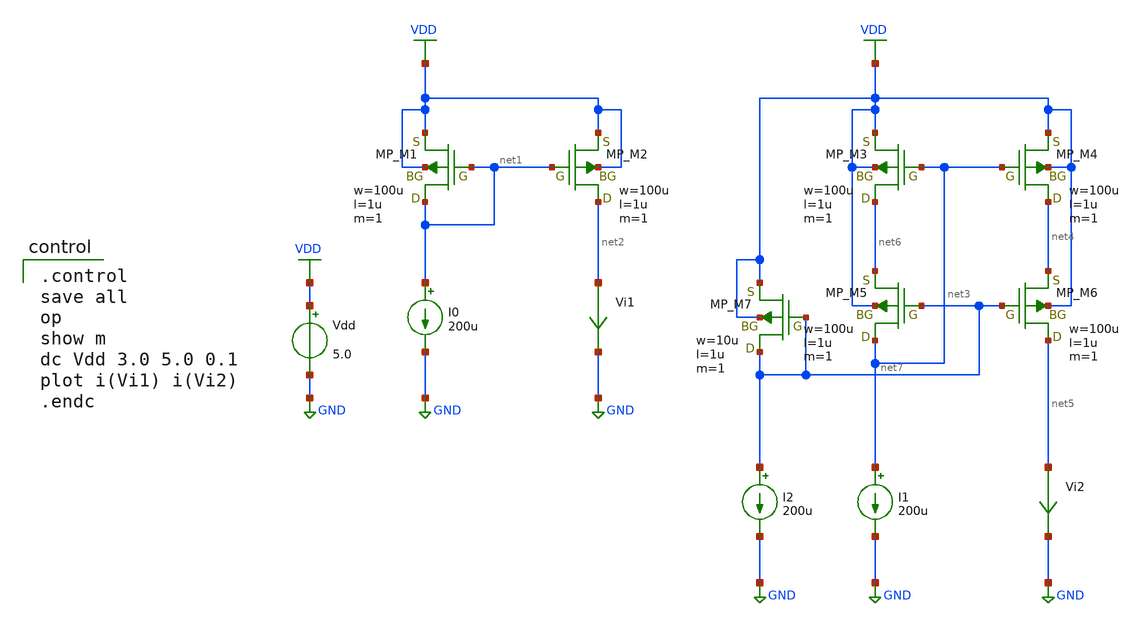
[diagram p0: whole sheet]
** sch_path: OpenSUSI-TR10/opamp/cascode.sch
**.subckt cascode
I0 net1 GND 200u
Vi1 net2 GND 0
.save i(vi1)
Vdd VDD GND 5.0
I1 net3 GND 200u
Vi2 net5 GND 0
.save i(vi2)
I2 net7 GND 200u
XM1 net1 net1 VDD VDD PMOS w=100u l=1u as=0 ad=0 ps=0 pd=0 nrd=0 nrs=0 m=1
XM2 net2 net1 VDD VDD PMOS w=100u l=1u as=0 ad=0 ps=0 pd=0 nrd=0 nrs=0 m=1
XM3 net6 net3 VDD VDD PMOS w=100u l=1u as=0 ad=0 ps=0 pd=0 nrd=0 nrs=0 m=1
XM4 net4 net3 VDD VDD PMOS w=100u l=1u as=0 ad=0 ps=0 pd=0 nrd=0 nrs=0 m=1
XM5 net3 net7 net6 VDD PMOS w=100u l=1u as=0 ad=0 ps=0 pd=0 nrd=0 nrs=0 m=1
XM6 net5 net7 net4 VDD PMOS w=100u l=1u as=0 ad=0 ps=0 pd=0 nrd=0 nrs=0 m=1
XM7 net7 net7 VDD VDD PMOS w=10u l=1u as=0 ad=0 ps=0 pd=0 nrd=0 nrs=0 m=1
**** begin user architecture code

.control
save all
op
show m
dc Vdd 3.0 5.0 0.1
plot i(Vi1) i(Vi2)
.endc

 .include $::LIB/ip62_models
**** end user architecture code
**.ends
.GLOBAL GND
.GLOBAL VDD
.end
